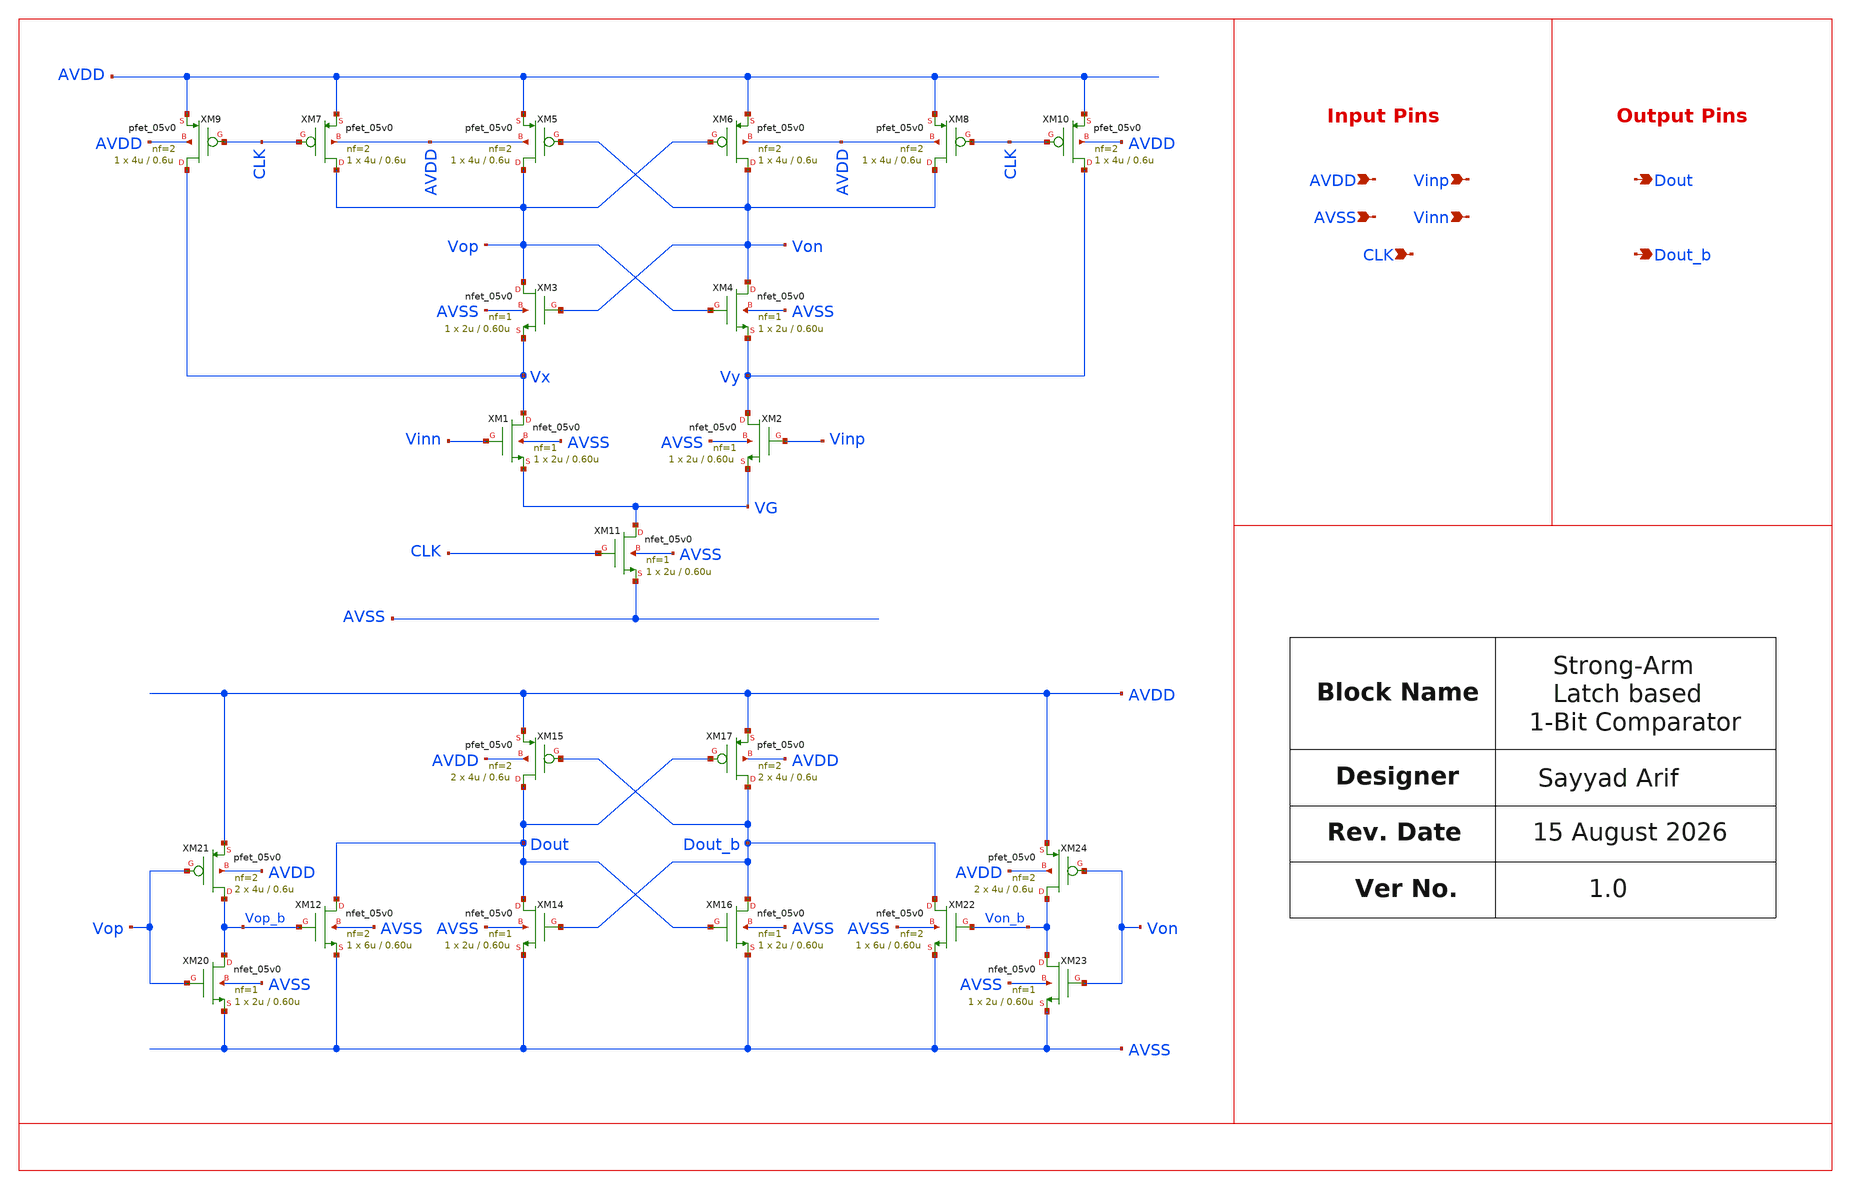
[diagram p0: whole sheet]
** sch_path: design/schematics/ADC/Quantizer/sa_cic_bms_afe_iadc_quantizer.sch
**.subckt sa_cic_bms_afe_iadc_quantizer Vinn Vinp AVSS AVDD CLK Dout_b Dout
*.ipin Vinn
*.ipin Vinp
*.ipin AVSS
*.ipin AVDD
*.ipin CLK
*.opin Dout_b
*.opin Dout
XM1 Vx Vinn VG AVSS nfet_05v0 L=0.60u W=2u nf=1 ad='int((nf+1)/2) * W/nf * 0.18u' as='int((nf+2)/2) * W/nf * 0.18u'
+ pd='2*int((nf+1)/2) * (W/nf + 0.18u)' ps='2*int((nf+2)/2) * (W/nf + 0.18u)' nrd='0.18u / W' nrs='0.18u / W'
+ sa=0 sb=0 sd=0 m=1
XM2 Vy Vinp VG AVSS nfet_05v0 L=0.60u W=2u nf=1 ad='int((nf+1)/2) * W/nf * 0.18u' as='int((nf+2)/2) * W/nf * 0.18u'
+ pd='2*int((nf+1)/2) * (W/nf + 0.18u)' ps='2*int((nf+2)/2) * (W/nf + 0.18u)' nrd='0.18u / W' nrs='0.18u / W'
+ sa=0 sb=0 sd=0 m=1
XM3 Vop Von Vx AVSS nfet_05v0 L=0.60u W=2u nf=1 ad='int((nf+1)/2) * W/nf * 0.18u' as='int((nf+2)/2) * W/nf * 0.18u'
+ pd='2*int((nf+1)/2) * (W/nf + 0.18u)' ps='2*int((nf+2)/2) * (W/nf + 0.18u)' nrd='0.18u / W' nrs='0.18u / W'
+ sa=0 sb=0 sd=0 m=1
XM4 Von Vop Vy AVSS nfet_05v0 L=0.60u W=2u nf=1 ad='int((nf+1)/2) * W/nf * 0.18u' as='int((nf+2)/2) * W/nf * 0.18u'
+ pd='2*int((nf+1)/2) * (W/nf + 0.18u)' ps='2*int((nf+2)/2) * (W/nf + 0.18u)' nrd='0.18u / W' nrs='0.18u / W'
+ sa=0 sb=0 sd=0 m=1
XM5 Vop Von AVDD AVDD pfet_05v0 L=0.6u W=4u nf=2 ad='int((nf+1)/2) * W/nf * 0.18u' as='int((nf+2)/2) * W/nf * 0.18u'
+ pd='2*int((nf+1)/2) * (W/nf + 0.18u)' ps='2*int((nf+2)/2) * (W/nf + 0.18u)' nrd='0.18u / W' nrs='0.18u / W'
+ sa=0 sb=0 sd=0 m=1
XM6 Von Vop AVDD AVDD pfet_05v0 L=0.6u W=4u nf=2 ad='int((nf+1)/2) * W/nf * 0.18u' as='int((nf+2)/2) * W/nf * 0.18u'
+ pd='2*int((nf+1)/2) * (W/nf + 0.18u)' ps='2*int((nf+2)/2) * (W/nf + 0.18u)' nrd='0.18u / W' nrs='0.18u / W'
+ sa=0 sb=0 sd=0 m=1
XM7 Vop CLK AVDD AVDD pfet_05v0 L=0.6u W=4u nf=2 ad='int((nf+1)/2) * W/nf * 0.18u' as='int((nf+2)/2) * W/nf * 0.18u'
+ pd='2*int((nf+1)/2) * (W/nf + 0.18u)' ps='2*int((nf+2)/2) * (W/nf + 0.18u)' nrd='0.18u / W' nrs='0.18u / W'
+ sa=0 sb=0 sd=0 m=1
XM8 Von CLK AVDD AVDD pfet_05v0 L=0.6u W=4u nf=2 ad='int((nf+1)/2) * W/nf * 0.18u' as='int((nf+2)/2) * W/nf * 0.18u'
+ pd='2*int((nf+1)/2) * (W/nf + 0.18u)' ps='2*int((nf+2)/2) * (W/nf + 0.18u)' nrd='0.18u / W' nrs='0.18u / W'
+ sa=0 sb=0 sd=0 m=1
XM9 Vx CLK AVDD AVDD pfet_05v0 L=0.6u W=4u nf=2 ad='int((nf+1)/2) * W/nf * 0.18u' as='int((nf+2)/2) * W/nf * 0.18u'
+ pd='2*int((nf+1)/2) * (W/nf + 0.18u)' ps='2*int((nf+2)/2) * (W/nf + 0.18u)' nrd='0.18u / W' nrs='0.18u / W'
+ sa=0 sb=0 sd=0 m=1
XM10 Vy CLK AVDD AVDD pfet_05v0 L=0.6u W=4u nf=2 ad='int((nf+1)/2) * W/nf * 0.18u' as='int((nf+2)/2) * W/nf * 0.18u'
+ pd='2*int((nf+1)/2) * (W/nf + 0.18u)' ps='2*int((nf+2)/2) * (W/nf + 0.18u)' nrd='0.18u / W' nrs='0.18u / W'
+ sa=0 sb=0 sd=0 m=1
XM11 VG CLK AVSS AVSS nfet_05v0 L=0.60u W=2u nf=1 ad='int((nf+1)/2) * W/nf * 0.18u' as='int((nf+2)/2) * W/nf * 0.18u'
+ pd='2*int((nf+1)/2) * (W/nf + 0.18u)' ps='2*int((nf+2)/2) * (W/nf + 0.18u)' nrd='0.18u / W' nrs='0.18u / W'
+ sa=0 sb=0 sd=0 m=1
XM12 Dout Vop_b AVSS AVSS nfet_05v0 L=0.60u W=6u nf=2 ad='int((nf+1)/2) * W/nf * 0.18u' as='int((nf+2)/2) * W/nf * 0.18u'
+ pd='2*int((nf+1)/2) * (W/nf + 0.18u)' ps='2*int((nf+2)/2) * (W/nf + 0.18u)' nrd='0.18u / W' nrs='0.18u / W'
+ sa=0 sb=0 sd=0 m=1
XM14 Dout Dout_b AVSS AVSS nfet_05v0 L=0.60u W=2u nf=1 ad='int((nf+1)/2) * W/nf * 0.18u' as='int((nf+2)/2) * W/nf * 0.18u'
+ pd='2*int((nf+1)/2) * (W/nf + 0.18u)' ps='2*int((nf+2)/2) * (W/nf + 0.18u)' nrd='0.18u / W' nrs='0.18u / W'
+ sa=0 sb=0 sd=0 m=1
XM15 Dout Dout_b AVDD AVDD pfet_05v0 L=0.6u W=4u nf=2 ad='int((nf+1)/2) * W/nf * 0.18u' as='int((nf+2)/2) * W/nf * 0.18u'
+ pd='2*int((nf+1)/2) * (W/nf + 0.18u)' ps='2*int((nf+2)/2) * (W/nf + 0.18u)' nrd='0.18u / W' nrs='0.18u / W'
+ sa=0 sb=0 sd=0 m=2
XM16 Dout_b Dout AVSS AVSS nfet_05v0 L=0.60u W=2u nf=1 ad='int((nf+1)/2) * W/nf * 0.18u' as='int((nf+2)/2) * W/nf * 0.18u'
+ pd='2*int((nf+1)/2) * (W/nf + 0.18u)' ps='2*int((nf+2)/2) * (W/nf + 0.18u)' nrd='0.18u / W' nrs='0.18u / W'
+ sa=0 sb=0 sd=0 m=1
XM17 Dout_b Dout AVDD AVDD pfet_05v0 L=0.6u W=4u nf=2 ad='int((nf+1)/2) * W/nf * 0.18u' as='int((nf+2)/2) * W/nf * 0.18u'
+ pd='2*int((nf+1)/2) * (W/nf + 0.18u)' ps='2*int((nf+2)/2) * (W/nf + 0.18u)' nrd='0.18u / W' nrs='0.18u / W'
+ sa=0 sb=0 sd=0 m=2
XM20 Vop_b Vop AVSS AVSS nfet_05v0 L=0.60u W=2u nf=1 ad='int((nf+1)/2) * W/nf * 0.18u' as='int((nf+2)/2) * W/nf * 0.18u'
+ pd='2*int((nf+1)/2) * (W/nf + 0.18u)' ps='2*int((nf+2)/2) * (W/nf + 0.18u)' nrd='0.18u / W' nrs='0.18u / W'
+ sa=0 sb=0 sd=0 m=1
XM21 Vop_b Vop AVDD AVDD pfet_05v0 L=0.6u W=4u nf=2 ad='int((nf+1)/2) * W/nf * 0.18u' as='int((nf+2)/2) * W/nf * 0.18u'
+ pd='2*int((nf+1)/2) * (W/nf + 0.18u)' ps='2*int((nf+2)/2) * (W/nf + 0.18u)' nrd='0.18u / W' nrs='0.18u / W'
+ sa=0 sb=0 sd=0 m=2
XM22 Dout_b Von_b AVSS AVSS nfet_05v0 L=0.60u W=6u nf=2 ad='int((nf+1)/2) * W/nf * 0.18u' as='int((nf+2)/2) * W/nf * 0.18u'
+ pd='2*int((nf+1)/2) * (W/nf + 0.18u)' ps='2*int((nf+2)/2) * (W/nf + 0.18u)' nrd='0.18u / W' nrs='0.18u / W'
+ sa=0 sb=0 sd=0 m=1
XM23 Von_b Von AVSS AVSS nfet_05v0 L=0.60u W=2u nf=1 ad='int((nf+1)/2) * W/nf * 0.18u' as='int((nf+2)/2) * W/nf * 0.18u'
+ pd='2*int((nf+1)/2) * (W/nf + 0.18u)' ps='2*int((nf+2)/2) * (W/nf + 0.18u)' nrd='0.18u / W' nrs='0.18u / W'
+ sa=0 sb=0 sd=0 m=1
XM24 Von_b Von AVDD AVDD pfet_05v0 L=0.6u W=4u nf=2 ad='int((nf+1)/2) * W/nf * 0.18u' as='int((nf+2)/2) * W/nf * 0.18u'
+ pd='2*int((nf+1)/2) * (W/nf + 0.18u)' ps='2*int((nf+2)/2) * (W/nf + 0.18u)' nrd='0.18u / W' nrs='0.18u / W'
+ sa=0 sb=0 sd=0 m=2
**.ends
.end
